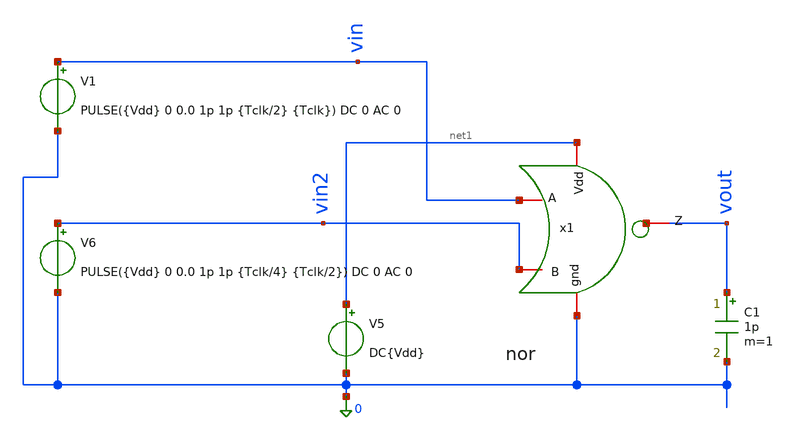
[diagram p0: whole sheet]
** sch_path: verification/testbenches/tb_nor.sch
**.subckt tb_nor
V5 net1 0 DC{Vdd}
V6 vin2 0 PULSE({Vdd} 0 0.0 1p 1p {Tclk/4} {Tclk/2}) DC 0 AC 0
V1 vin 0 PULSE({Vdd} 0 0.0 1p 1p {Tclk/2} {Tclk}) DC 0 AC 0
C1 vout 0 1p m=1
x1 net1 vin vout vin2 0 nor
**** begin user architecture code


* Circuit Parameters
.param Vdd = 1.2
.param Tclk = 20n
.options TEMP = 27.0
* Include Models - IHP SG13G2
.lib cornerMOSlv.lib mos_tt
* OP Parameters & Singals to save
.save all
*Simulations
.control
tran 0.01u 100n
setplot tran1
plot v(vin) v(vin2)+1.2 v(vout)+2.4
reset
dc V6 0 1.2 0.01
dc V1 0 1.2 0.01
setplot dc
plot vin vout ylabel vout xlabel vin
set filetype = ascii
write dcsweep.raw
.endc
.end


**** end user architecture code
**.ends

* expanding   symbol:  blocks/nor/schematic/nor.sym # of pins=5
** sym_path: design/blocks/nor/schematic/nor.sym
** sch_path: design/blocks/nor/schematic/nor.sch
.subckt nor Vdd A Z B gnd
*.iopin A
*.iopin B
*.iopin Vdd
*.iopin Z
*.iopin gnd
XM2 gnd A Z gnd sg13_lv_nmos w=1.5u l=0.15u ng=1 m=1 mm_ok=1
XM3 Z B gnd gnd sg13_lv_nmos w=1.5u l=0.15u ng=1 m=1 mm_ok=1
XM0 Z B net1 Vdd sg13_lv_pmos w=1.5u l=0.15u ng=1 m=1 mm_ok=1
XM1 Vdd A net1 Vdd sg13_lv_pmos w=1.5u l=0.15u ng=1 m=1 mm_ok=1
.ends

.end
